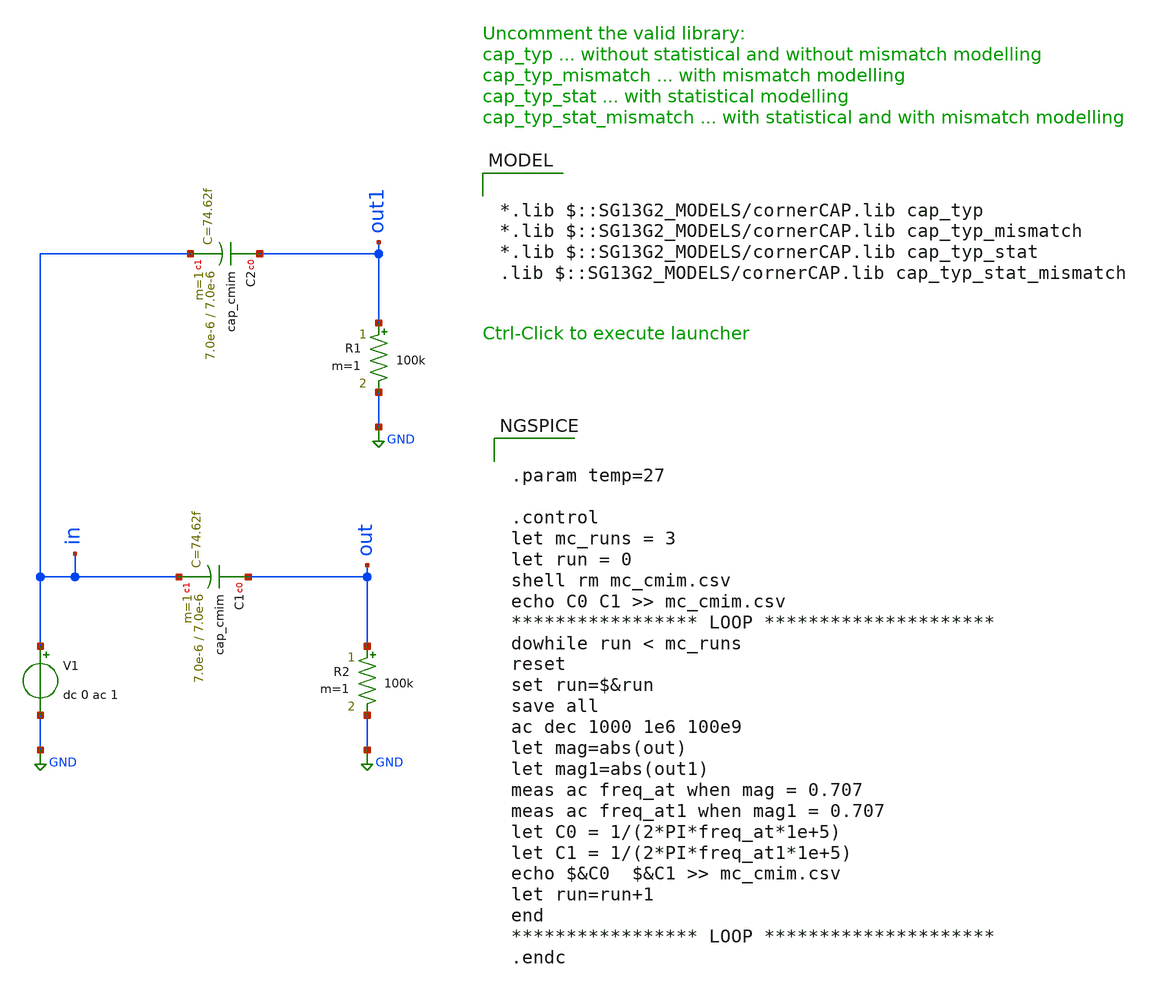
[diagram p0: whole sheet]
** sch_path: ihp-sg13g2/libs.tech/xschem/sg13g2_tests/mc_mim_cap_ac.sch
* Copyright 2021 Stefan Frederik Schippers
* Licensed under the Apache License, Version 2.0 (the "License");
* you may not use this file except in compliance with the License.
* You may obtain a copy of the License at
* https://www.apache.org/licenses/LICENSE-2.0
* Unless required by applicable law or agreed to in writing, software
* distributed under the License is distributed on an "AS IS" BASIS,
* WITHOUT WARRANTIES OR CONDITIONS OF ANY KIND, either express or implied.
* See the License for the specific language governing permissions and
* limitations under the License.
* Copyright 2023 IHP PDK Authors
**.subckt mc_mim_cap_ac
V1 in GND dc 0 ac 1
R2 out GND 100k m=1
XC1 out in cap_cmim w=7.0e-6 l=7.0e-6 m=1
R1 out1 GND 100k m=1
XC2 out1 in cap_cmim w=7.0e-6 l=7.0e-6 m=1
**** begin user architecture code


.param temp=27

.control
let mc_runs = 3
let run = 0
shell rm mc_cmim.csv
echo C0 C1 >> mc_cmim.csv
***************** LOOP *********************
dowhile run < mc_runs
reset
set run=$&run
save all
ac dec 1000 1e6 100e9
let mag=abs(out)
let mag1=abs(out1)
meas ac freq_at when mag = 0.707
meas ac freq_at1 when mag1 = 0.707
let C0 = 1/(2*PI*freq_at*1e+5)
let C1 = 1/(2*PI*freq_at1*1e+5)
echo $&C0  $&C1 >> mc_cmim.csv
let run=run+1
end
***************** LOOP *********************
.endc



*.lib $::SG13G2_MODELS/cornerCAP.lib cap_typ
*.lib $::SG13G2_MODELS/cornerCAP.lib cap_typ_mismatch
*.lib $::SG13G2_MODELS/cornerCAP.lib cap_typ_stat
.lib $::SG13G2_MODELS/cornerCAP.lib cap_typ_stat_mismatch

**** end user architecture code
**.ends
.GLOBAL GND
.end
